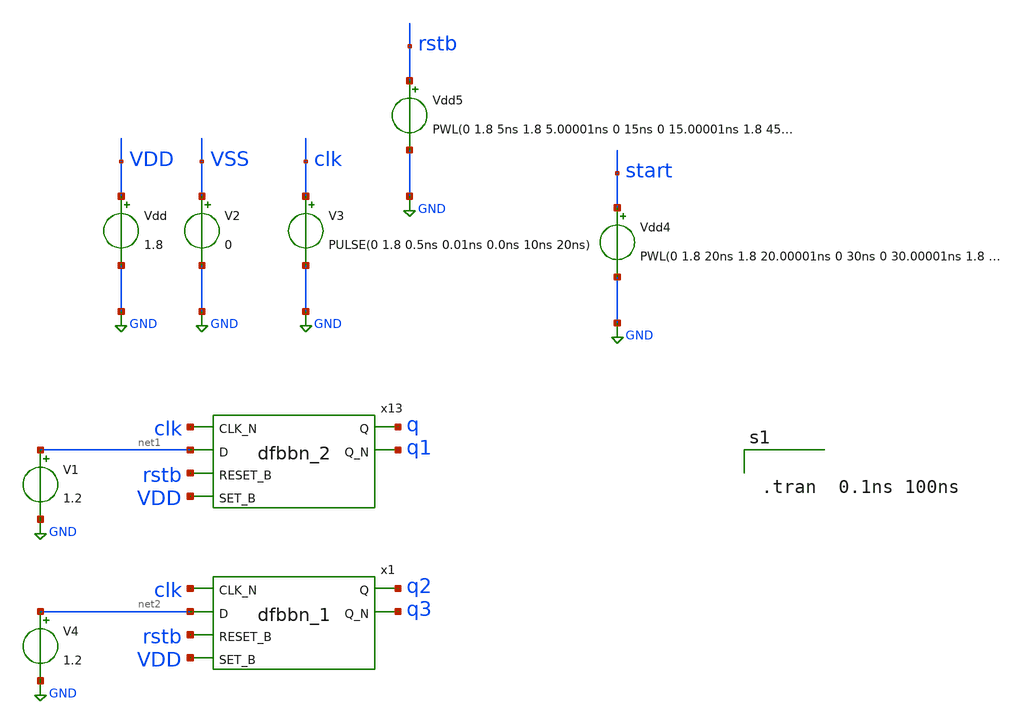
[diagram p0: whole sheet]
** sch_path: dff_tb.sch
**.subckt dff_tb
x13 clk net1 rstb VDD VSS VNB VPB VDD q q1 sky130_fd_sc_hd__dfbbn_2
Vdd VDD GND 1.8
V2 VSS GND 0
Vdd4 start GND PWL(0 1.8 20ns 1.8 20.00001ns 0 30ns 0 30.00001ns 1.8 50ns 1.8 50.00001ns 0 60ns 0
+ 60.00001ns 1.8 )
Vdd5 rstb GND PWL(0 1.8 5ns 1.8 5.00001ns 0 15ns 0 15.00001ns 1.8 45ns 1.8 45.00001ns 0 55ns 0
+ 55.00001ns 1.8)
V3 clk GND PULSE(0 1.8 0.5ns 0.01ns 0.0ns 10ns 20ns)
V1 net1 GND 1.2
x1 clk net2 rstb VDD VGND VNB VPB VPWR q2 q3 sky130_fd_sc_hd__dfbbn_1
V4 net2 GND 1.2
**** begin user architecture code

** opencircuitdesign pdks install
.lib $::SKYWATER_MODELS/sky130.lib.spice tt
.include $::SKYWATER_STDCELLS/sky130_fd_sc_hd.spice




.tran  0.1ns 100ns





**** end user architecture code
**.ends
.GLOBAL GND
.end
